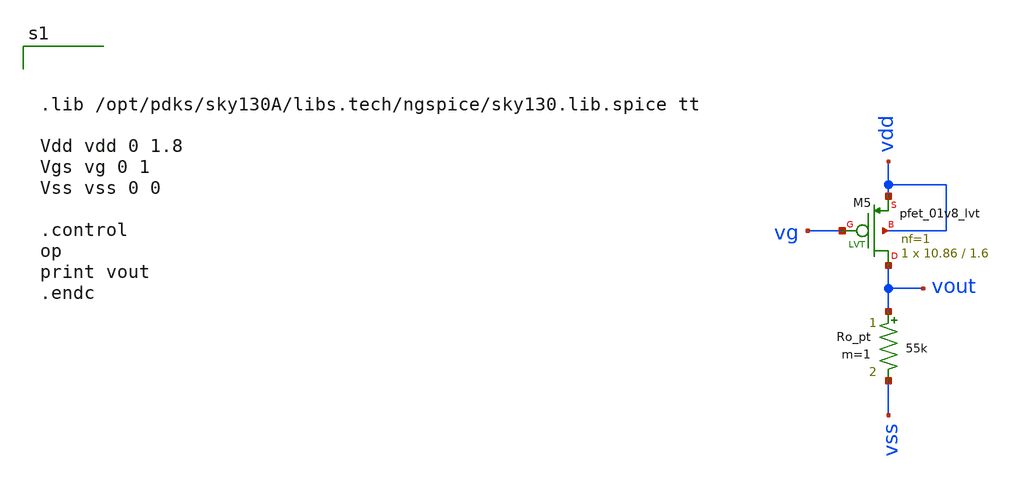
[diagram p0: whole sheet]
** sch_path: test-python/sstadex/untitled-2.sch
**.subckt untitled-2
XM5 vout vg vdd vdd sky130_fd_pr__pfet_01v8_lvt L=1.6 W=10.86 nf=1 ad='int((nf+1)/2) * W/nf * 0.29' as='int((nf+2)/2) * W/nf * 0.29'
+ pd='2*int((nf+1)/2) * (W/nf + 0.29)' ps='2*int((nf+2)/2) * (W/nf + 0.29)' nrd='0.29 / W' nrs='0.29 / W'
+ sa=0 sb=0 sd=0 mult=1 m=1
Ro_pt vout vss 55k m=1
**** begin user architecture code



.lib /opt/pdks/sky130A/libs.tech/ngspice/sky130.lib.spice tt

Vdd vdd 0 1.8
Vgs vg 0 1
Vss vss 0 0

.control
op
print vout
.endc



**** end user architecture code
**.ends
.end
